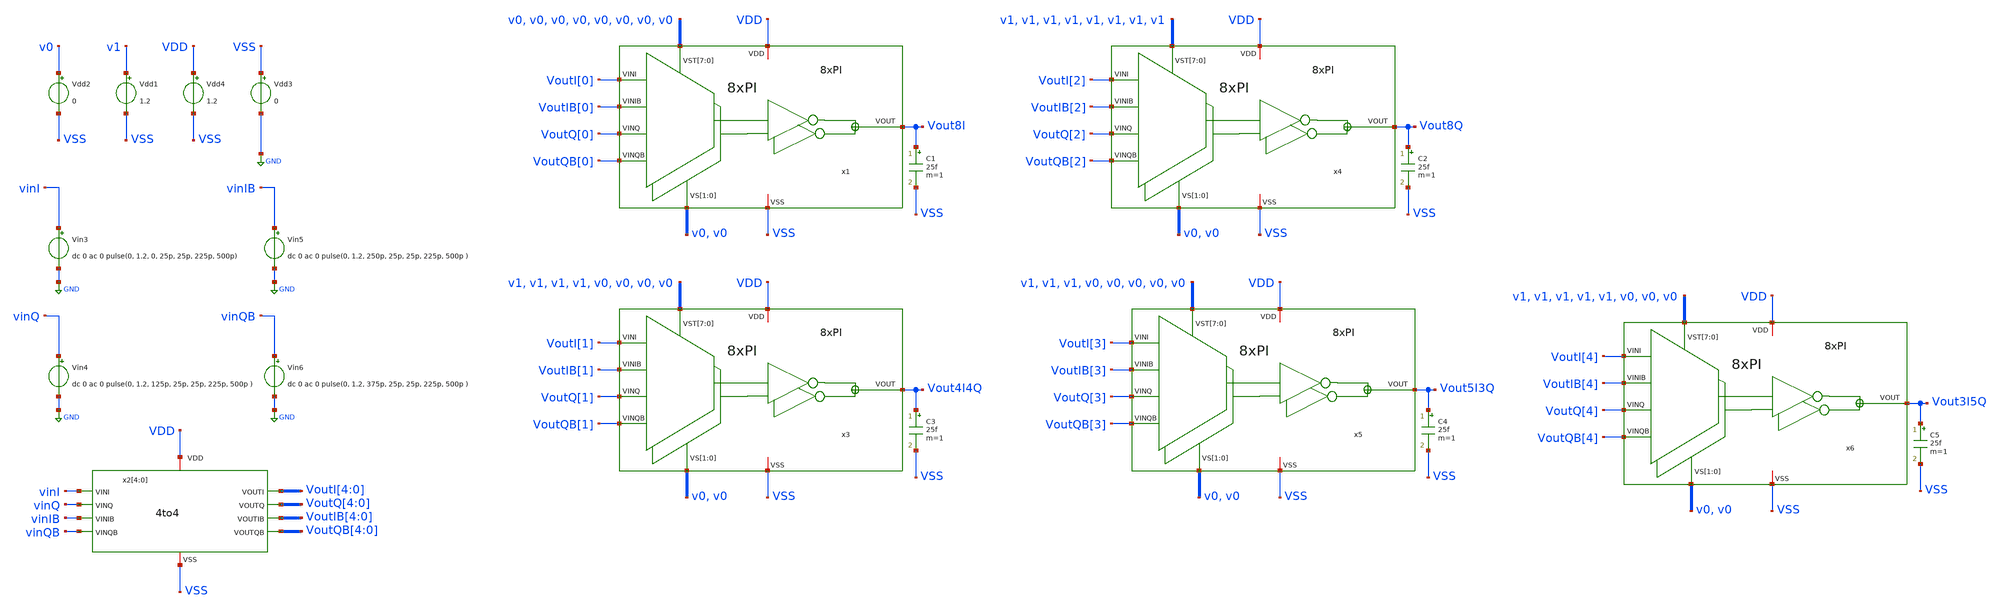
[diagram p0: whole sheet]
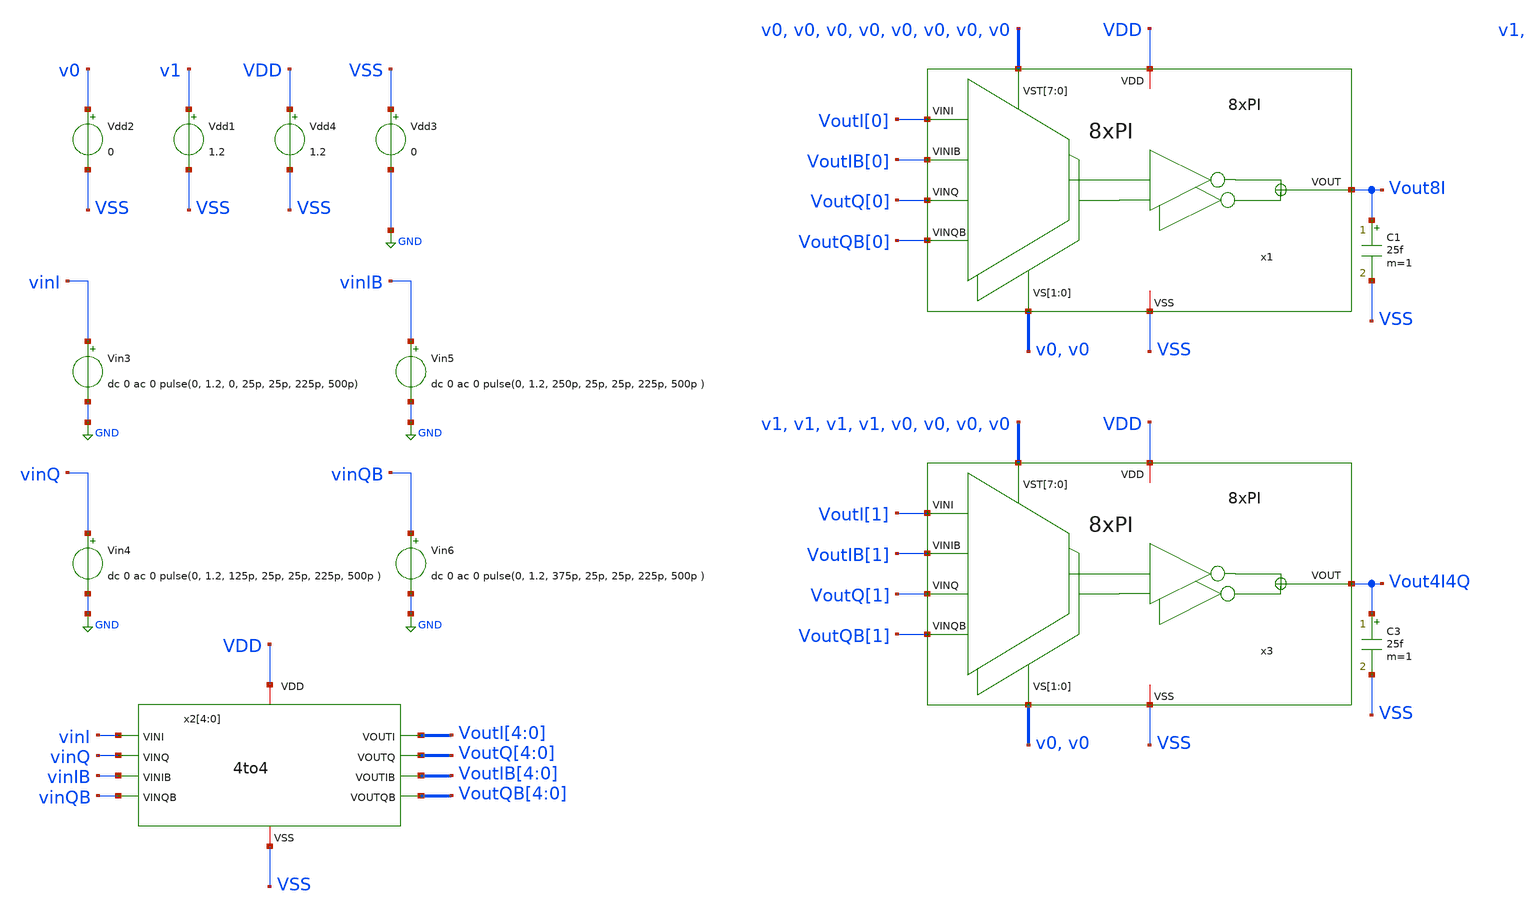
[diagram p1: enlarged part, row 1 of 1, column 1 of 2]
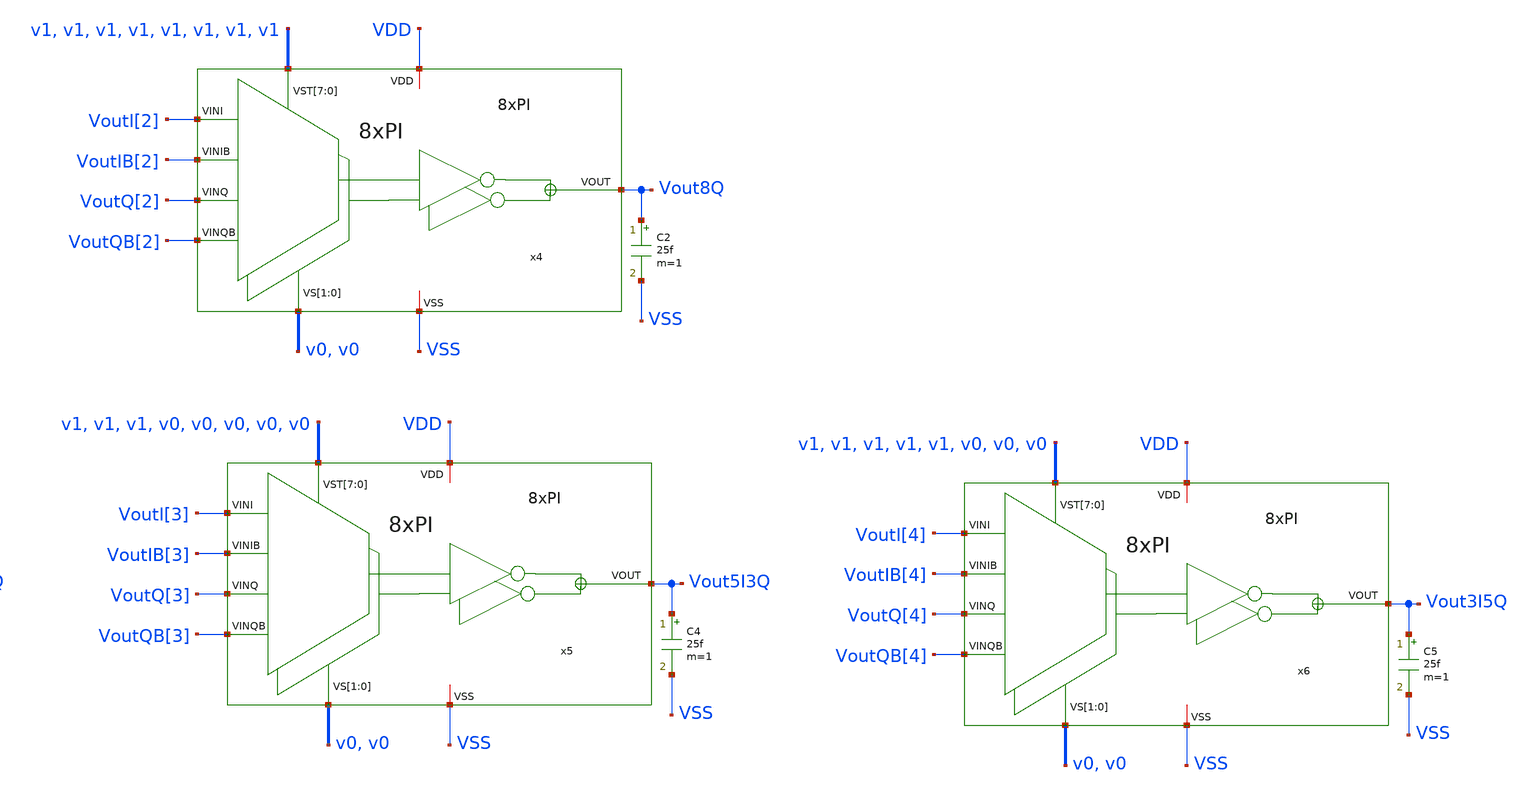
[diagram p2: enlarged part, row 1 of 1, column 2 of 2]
** sch_path: CDR4176-main/testbenches/tran/xschem/tb_8xPI.sch
**.subckt tb_8xPI
x1 VoutI[0] VoutIB[0] VoutQ[0] VoutQB[0] v0 v0 v0 v0 v0 v0 v0 v0 v0 v0 Vout8I VDD VSS 8xPI
Vin3 vinI GND dc 0 ac 0 pulse(0, 1.2, 0, 25p, 25p, 225p, 500p)
Vin4 vinQ GND dc 0 ac 0 pulse(0, 1.2, 125p, 25p, 25p, 225p, 500p )
Vin5 vinIB GND dc 0 ac 0 pulse(0, 1.2, 250p, 25p, 25p, 225p, 500p )
Vin6 vinQB GND dc 0 ac 0 pulse(0, 1.2, 375p, 25p, 25p, 225p, 500p )
x2[4] VDD vinI VoutI[4] VoutQ[4] vinQ vinIB VoutIB[4] vinQB VoutQB[4] VSS 4to4
x2[3] VDD vinI VoutI[3] VoutQ[3] vinQ vinIB VoutIB[3] vinQB VoutQB[3] VSS 4to4
x2[2] VDD vinI VoutI[2] VoutQ[2] vinQ vinIB VoutIB[2] vinQB VoutQB[2] VSS 4to4
x2[1] VDD vinI VoutI[1] VoutQ[1] vinQ vinIB VoutIB[1] vinQB VoutQB[1] VSS 4to4
x2[0] VDD vinI VoutI[0] VoutQ[0] vinQ vinIB VoutIB[0] vinQB VoutQB[0] VSS 4to4
Vdd4 VDD VSS 1.2
Vdd1 v1 VSS 1.2
Vdd2 v0 VSS 0
Vdd3 VSS GND 0
x3 VoutI[1] VoutIB[1] VoutQ[1] VoutQB[1] v0 v0 v1 v1 v1 v1 v0 v0 v0 v0 Vout4I4Q VDD VSS 8xPI
x4 VoutI[2] VoutIB[2] VoutQ[2] VoutQB[2] v0 v0 v1 v1 v1 v1 v1 v1 v1 v1 Vout8Q VDD VSS 8xPI
x5 VoutI[3] VoutIB[3] VoutQ[3] VoutQB[3] v0 v0 v1 v1 v1 v0 v0 v0 v0 v0 Vout5I3Q VDD VSS 8xPI
x6 VoutI[4] VoutIB[4] VoutQ[4] VoutQB[4] v0 v0 v1 v1 v1 v1 v1 v0 v0 v0 Vout3I5Q VDD VSS 8xPI
C1 Vout8I VSS 25f m=1
C2 Vout8Q VSS 25f m=1
C3 Vout4I4Q VSS 25f m=1
C4 Vout5I3Q VSS 25f m=1
C5 Vout3I5Q VSS 25f m=1
**** begin user architecture code


.param temp=27
.control
save all
tran 5p 1.5n

*meas tran tPWI TRIG v(Vout_I) VAl=0.6 RISE=1 TARG v(Vout_I) VAl=0.6 FALL=1
*meas tran tPWIQ TRIG v(Vout_IQ) VAl=0.6 RISE=1 TARG v(Vout_IQ) VAl=0.6 FALL=1
*meas tran tPWQ TRIG v(Vout_Q) VAl=0.6 RISE=1 TARG v(Vout_Q) VAl=0.6 FALL=1
*meas tran tPWQIB TRIG v(Vout_QIB) VAl=0.6 RISE=1 TARG v(Vout_QIB) VAl=0.6 FALL=1
*meas tran tPWIB TRIG v(Vout_IB) VAl=0.6 RISE=1 TARG v(Vout_IB) VAl=0.6 FALL=1
*meas tran tPWIBQB TRIG v(Vout_IBQB) VAl=0.6 RISE=1 TARG v(Vout_IBQB) VAl=0.6 FALL=1
*meas tran tPWQB TRIG v(Vout_QB) VAl=0.6 RISE=1 TARG v(Vout_QB) VAl=0.6 FALL=1
*meas tran tPWQBI TRIG v(Vout_QBI) VAl=0.6 RISE=1 TARG v(Vout_QBI) VAl=0.6 FALL=1


*meas tran tskewI_IQ TRIG v(Vout_I) VAl=0.6 RISE=1 TARG v(Vout_IQ) VAl=0.6 RISE=1
*meas tran tskewIQ_Q TRIG v(Vout_IQ) VAl=0.6 RISE=1 TARG v(Vout_Q) VAl=0.6 RISE=1
*meas tran tskewQ_QIB TRIG v(Vout_Q) VAl=0.6 RISE=1 TARG v(Vout_QIB) VAl=0.6 RISE=1
*meas tran tskewQIB_IB TRIG v(Vout_QIB) VAl=0.6 RISE=1 TARG v(Vout_IB) VAl=0.6 RISE=1
*meas tran tskewIB_IBQB TRIG v(Vout_IB) VAl=0.6 RISE=1 TARG v(Vout_IBQB) VAl=0.6 RISE=1
*meas tran tskewIBQB_QB TRIG v(Vout_IBQB) VAl=0.6 RISE=1 TARG v(Vout_QB) VAl=0.6 RISE=1
*meas tran tskewQB_QBI TRIG v(Vout_QB) VAl=0.6 RISE=1 TARG v(Vout_QBI) VAl=0.6 RISE=1
*meas tran tskewQBI_I TRIG v(Vout_QBI) VAl=0.6 RISE=1 TARG v(Vout_I) VAl=0.6 RISE=2


write tran_8XPI.raw
.endc



.lib cornerMOSlv.lib mos_tt

**** end user architecture code
**.ends
.GLOBAL GND
.end
